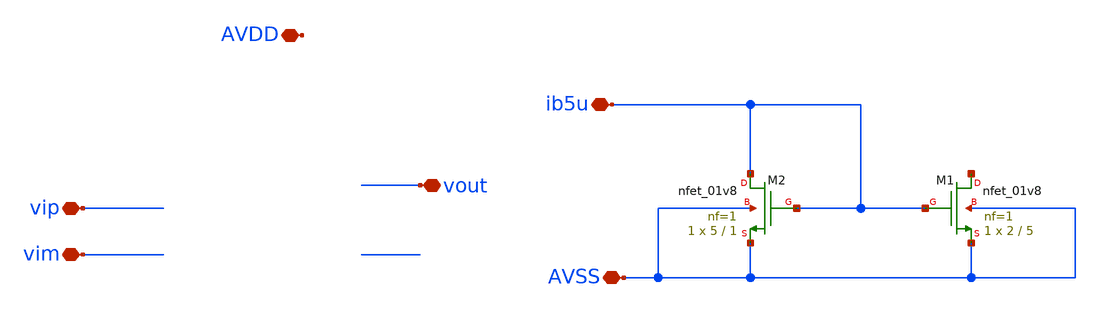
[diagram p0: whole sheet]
** sch_path: xschem/opa_nmos1.sch
**.subckt opa_nmos1 vip vim vout ib5u AVDD AVSS
*.iopin vip
*.iopin vim
*.iopin vout
*.iopin ib5u
*.iopin AVDD
*.iopin AVSS
XM2 ib5u ib5u AVSS AVSS sky130_fd_pr__nfet_01v8 L=1 W=5 nf=1 ad='int((1 + 1)/2) * 5 / 1 * 0.29' as='int((1 + 2)/2) * 5 / 1 * 0.29'
+ pd='2*int((1 + 1)/2) * (5 / 1 + 0.29)' ps='2*int((1 + 2)/2) * (5 / 1 + 0.29)' nrd='0.29 / 5 ' nrs='0.29 / 5 '
+ sa=0 sb=0 sd=0 mult=1 m=1
XM1 net2 ib5u AVSS AVSS sky130_fd_pr__nfet_01v8 L=5 W=2 nf=1 ad='int((1 + 1)/2) * 2 / 1 * 0.29' as='int((1 + 2)/2) * 2 / 1 * 0.29'
+ pd='2*int((1 + 1)/2) * (2 / 1 + 0.29)' ps='2*int((1 + 2)/2) * (2 / 1 + 0.29)' nrd='0.29 / 2 ' nrs='0.29 / 2 '
+ sa=0 sb=0 sd=0 mult=1 m=1
**.ends
.end
